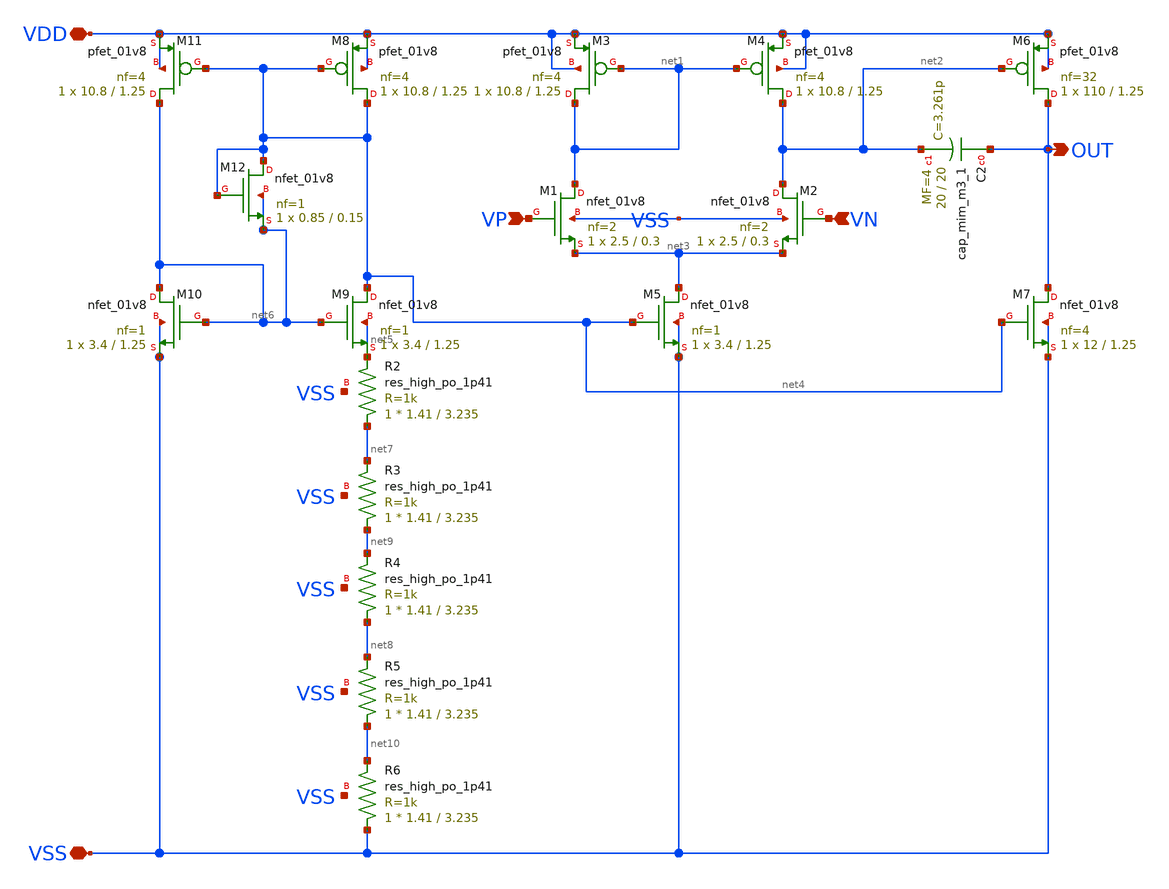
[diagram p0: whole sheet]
** sch_path: bandgap/bgr-opamp/bgr-opamp.sch
**.subckt bgr-opamp VSS VDD VP VN OUT
*.iopin VSS
*.iopin VDD
*.ipin VP
*.ipin VN
*.opin OUT
XM1 net1 VP net3 VSS sky130_fd_pr__nfet_01v8 L=0.3 W=2.5 nf=2 ad='int((nf+1)/2) * W/nf * 0.29' as='int((nf+2)/2) * W/nf * 0.29'
+ pd='2*int((nf+1)/2) * (W/nf + 0.29)' ps='2*int((nf+2)/2) * (W/nf + 0.29)' nrd='0.29 / W' nrs='0.29 / W'
+ sa=0 sb=0 sd=0 mult=1 m=1
XM2 net2 VN net3 VSS sky130_fd_pr__nfet_01v8 L=0.3 W=2.5 nf=2 ad='int((nf+1)/2) * W/nf * 0.29' as='int((nf+2)/2) * W/nf * 0.29'
+ pd='2*int((nf+1)/2) * (W/nf + 0.29)' ps='2*int((nf+2)/2) * (W/nf + 0.29)' nrd='0.29 / W' nrs='0.29 / W'
+ sa=0 sb=0 sd=0 mult=1 m=1
XM4 net2 net1 VDD VDD sky130_fd_pr__pfet_01v8 L=1.25 W=10.8 nf=4 ad='int((nf+1)/2) * W/nf * 0.29' as='int((nf+2)/2) * W/nf * 0.29'
+ pd='2*int((nf+1)/2) * (W/nf + 0.29)' ps='2*int((nf+2)/2) * (W/nf + 0.29)' nrd='0.29 / W' nrs='0.29 / W'
+ sa=0 sb=0 sd=0 mult=1 m=1
XM3 net1 net1 VDD VDD sky130_fd_pr__pfet_01v8 L=1.25 W=10.8 nf=4 ad='int((nf+1)/2) * W/nf * 0.29' as='int((nf+2)/2) * W/nf * 0.29'
+ pd='2*int((nf+1)/2) * (W/nf + 0.29)' ps='2*int((nf+2)/2) * (W/nf + 0.29)' nrd='0.29 / W' nrs='0.29 / W'
+ sa=0 sb=0 sd=0 mult=1 m=1
XM5 net3 net4 VSS VSS sky130_fd_pr__nfet_01v8 L=1.25 W=3.4 nf=1 ad='int((nf+1)/2) * W/nf * 0.29' as='int((nf+2)/2) * W/nf * 0.29'
+ pd='2*int((nf+1)/2) * (W/nf + 0.29)' ps='2*int((nf+2)/2) * (W/nf + 0.29)' nrd='0.29 / W' nrs='0.29 / W'
+ sa=0 sb=0 sd=0 mult=1 m=1
XM9 net4 net6 net5 net5 sky130_fd_pr__nfet_01v8 L=1.25 W=3.4 nf=1 ad='int((nf+1)/2) * W/nf * 0.29' as='int((nf+2)/2) * W/nf * 0.29'
+ pd='2*int((nf+1)/2) * (W/nf + 0.29)' ps='2*int((nf+2)/2) * (W/nf + 0.29)' nrd='0.29 / W' nrs='0.29 / W'
+ sa=0 sb=0 sd=0 mult=1 m=1
XM8 net4 net4 VDD VDD sky130_fd_pr__pfet_01v8 L=1.25 W=10.8 nf=4 ad='int((nf+1)/2) * W/nf * 0.29' as='int((nf+2)/2) * W/nf * 0.29'
+ pd='2*int((nf+1)/2) * (W/nf + 0.29)' ps='2*int((nf+2)/2) * (W/nf + 0.29)' nrd='0.29 / W' nrs='0.29 / W'
+ sa=0 sb=0 sd=0 mult=1 m=1
XM11 net6 net4 VDD VDD sky130_fd_pr__pfet_01v8 L=1.25 W=10.8 nf=4 ad='int((nf+1)/2) * W/nf * 0.29' as='int((nf+2)/2) * W/nf * 0.29'
+ pd='2*int((nf+1)/2) * (W/nf + 0.29)' ps='2*int((nf+2)/2) * (W/nf + 0.29)' nrd='0.29 / W' nrs='0.29 / W'
+ sa=0 sb=0 sd=0 mult=1 m=1
XM10 net6 net6 VSS VSS sky130_fd_pr__nfet_01v8 L=1.25 W=3.4 nf=1 ad='int((nf+1)/2) * W/nf * 0.29' as='int((nf+2)/2) * W/nf * 0.29'
+ pd='2*int((nf+1)/2) * (W/nf + 0.29)' ps='2*int((nf+2)/2) * (W/nf + 0.29)' nrd='0.29 / W' nrs='0.29 / W'
+ sa=0 sb=0 sd=0 mult=1 m=1
XM6 OUT net2 VDD VDD sky130_fd_pr__pfet_01v8 L=1.25 W=110 nf=32 ad='int((nf+1)/2) * W/nf * 0.29' as='int((nf+2)/2) * W/nf * 0.29'
+ pd='2*int((nf+1)/2) * (W/nf + 0.29)' ps='2*int((nf+2)/2) * (W/nf + 0.29)' nrd='0.29 / W' nrs='0.29 / W'
+ sa=0 sb=0 sd=0 mult=1 m=1
XM7 OUT net4 VSS VSS sky130_fd_pr__nfet_01v8 L=1.25 W=12 nf=4 ad='int((nf+1)/2) * W/nf * 0.29' as='int((nf+2)/2) * W/nf * 0.29'
+ pd='2*int((nf+1)/2) * (W/nf + 0.29)' ps='2*int((nf+2)/2) * (W/nf + 0.29)' nrd='0.29 / W' nrs='0.29 / W'
+ sa=0 sb=0 sd=0 mult=1 m=1
XC2 OUT net2 sky130_fd_pr__cap_mim_m3_1 W=20 L=20 MF=4 m=4
XM12 net4 net4 net6 net6 sky130_fd_pr__nfet_01v8 L=0.15 W=0.85 nf=1 ad='int((nf+1)/2) * W/nf * 0.29'
+ as='int((nf+2)/2) * W/nf * 0.29' pd='2*int((nf+1)/2) * (W/nf + 0.29)' ps='2*int((nf+2)/2) * (W/nf + 0.29)'
+ nrd='0.29 / W' nrs='0.29 / W' sa=0 sb=0 sd=0 mult=1 m=1
XR2 net7 net5 VSS sky130_fd_pr__res_high_po_1p41 L=3.235 mult=1 m=1
XR3 net9 net7 VSS sky130_fd_pr__res_high_po_1p41 L=3.235 mult=1 m=1
XR4 net8 net9 VSS sky130_fd_pr__res_high_po_1p41 L=3.235 mult=1 m=1
XR5 net10 net8 VSS sky130_fd_pr__res_high_po_1p41 L=3.235 mult=1 m=1
XR6 VSS net10 VSS sky130_fd_pr__res_high_po_1p41 L=3.235 mult=1 m=1
**.ends
.end
